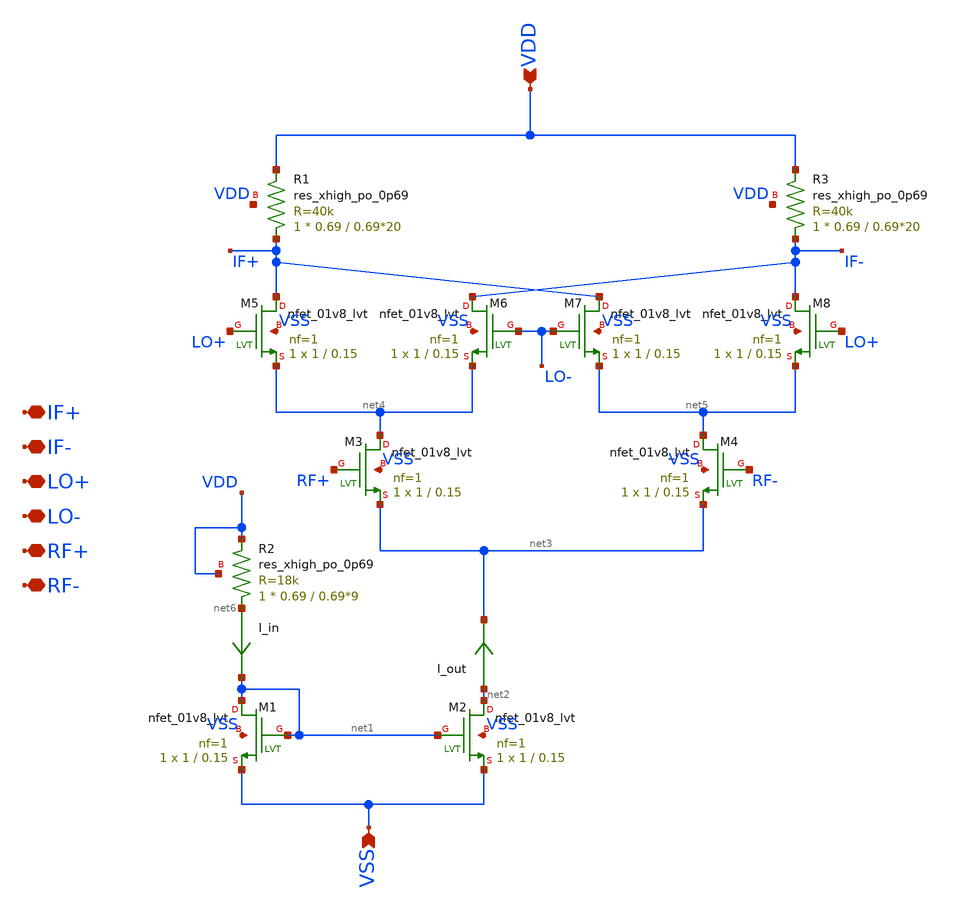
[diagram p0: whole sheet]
** sch_path: hw03/xschem/gill_cell.sch
**.subckt gill_cell VSS VDD IF+ IF- LO+ LO- RF+ RF-
*.ipin VSS
*.ipin VDD
*.iopin IF+
*.iopin IF-
*.iopin LO+
*.iopin LO-
*.iopin RF+
*.iopin RF-
XM1 net1 net1 VSS VSS sky130_fd_pr__nfet_01v8_lvt L=0.15 W=1 nf=1 ad='int((1 + 1)/2) * 1 / 1 * 0.29'
+ as='int((1 + 2)/2) * 1 / 1 * 0.29' pd='2*int((1 + 1)/2) * (1 / 1 + 0.29)' ps='2*int((1 + 2)/2) * (1 / 1 + 0.29)'
+ nrd='0.29 / 1 ' nrs='0.29 / 1 ' sa=0 sb=0 sd=0 mult=1 m=1
XM2 net2 net1 VSS VSS sky130_fd_pr__nfet_01v8_lvt L=0.15 W=1 nf=1 ad='int((1 + 1)/2) * 1 / 1 * 0.29'
+ as='int((1 + 2)/2) * 1 / 1 * 0.29' pd='2*int((1 + 1)/2) * (1 / 1 + 0.29)' ps='2*int((1 + 2)/2) * (1 / 1 + 0.29)'
+ nrd='0.29 / 1 ' nrs='0.29 / 1 ' sa=0 sb=0 sd=0 mult=1 m=1
I_in net6 net1 0
.save i(i_in)
I_out net2 net3 0
.save i(i_out)
XM3 net4 RF+ net3 VSS sky130_fd_pr__nfet_01v8_lvt L=0.15 W=1 nf=1 ad='int((1 + 1)/2) * 1 / 1 * 0.29'
+ as='int((1 + 2)/2) * 1 / 1 * 0.29' pd='2*int((1 + 1)/2) * (1 / 1 + 0.29)' ps='2*int((1 + 2)/2) * (1 / 1 + 0.29)'
+ nrd='0.29 / 1 ' nrs='0.29 / 1 ' sa=0 sb=0 sd=0 mult=1 m=1
XM4 net5 RF- net3 VSS sky130_fd_pr__nfet_01v8_lvt L=0.15 W=1 nf=1 ad='int((1 + 1)/2) * 1 / 1 * 0.29'
+ as='int((1 + 2)/2) * 1 / 1 * 0.29' pd='2*int((1 + 1)/2) * (1 / 1 + 0.29)' ps='2*int((1 + 2)/2) * (1 / 1 + 0.29)'
+ nrd='0.29 / 1 ' nrs='0.29 / 1 ' sa=0 sb=0 sd=0 mult=1 m=1
XM5 IF+ LO+ net4 VSS sky130_fd_pr__nfet_01v8_lvt L=0.15 W=1 nf=1 ad='int((1 + 1)/2) * 1 / 1 * 0.29' as='int((1 + 2)/2) * 1 / 1 * 0.29'
+ pd='2*int((1 + 1)/2) * (1 / 1 + 0.29)' ps='2*int((1 + 2)/2) * (1 / 1 + 0.29)' nrd='0.29 / 1 ' nrs='0.29 / 1 '
+ sa=0 sb=0 sd=0 mult=1 m=1
XM6 IF- LO- net4 VSS sky130_fd_pr__nfet_01v8_lvt L=0.15 W=1 nf=1 ad='int((1 + 1)/2) * 1 / 1 * 0.29' as='int((1 + 2)/2) * 1 / 1 * 0.29'
+ pd='2*int((1 + 1)/2) * (1 / 1 + 0.29)' ps='2*int((1 + 2)/2) * (1 / 1 + 0.29)' nrd='0.29 / 1 ' nrs='0.29 / 1 '
+ sa=0 sb=0 sd=0 mult=1 m=1
XM7 IF+ LO- net5 VSS sky130_fd_pr__nfet_01v8_lvt L=0.15 W=1 nf=1 ad='int((1 + 1)/2) * 1 / 1 * 0.29' as='int((1 + 2)/2) * 1 / 1 * 0.29'
+ pd='2*int((1 + 1)/2) * (1 / 1 + 0.29)' ps='2*int((1 + 2)/2) * (1 / 1 + 0.29)' nrd='0.29 / 1 ' nrs='0.29 / 1 '
+ sa=0 sb=0 sd=0 mult=1 m=1
XM8 IF- LO+ net5 VSS sky130_fd_pr__nfet_01v8_lvt L=0.15 W=1 nf=1 ad='int((1 + 1)/2) * 1 / 1 * 0.29' as='int((1 + 2)/2) * 1 / 1 * 0.29'
+ pd='2*int((1 + 1)/2) * (1 / 1 + 0.29)' ps='2*int((1 + 2)/2) * (1 / 1 + 0.29)' nrd='0.29 / 1 ' nrs='0.29 / 1 '
+ sa=0 sb=0 sd=0 mult=1 m=1
XR1 IF+ VDD VDD sky130_fd_pr__res_xhigh_po_0p69 L=0.69*20 mult=1 m=1
XR3 IF- VDD VDD sky130_fd_pr__res_xhigh_po_0p69 L=0.69*20 mult=1 m=1
XR2 net6 VDD VDD sky130_fd_pr__res_xhigh_po_0p69 L=0.69*9 mult=1 m=1
**.ends
.end
